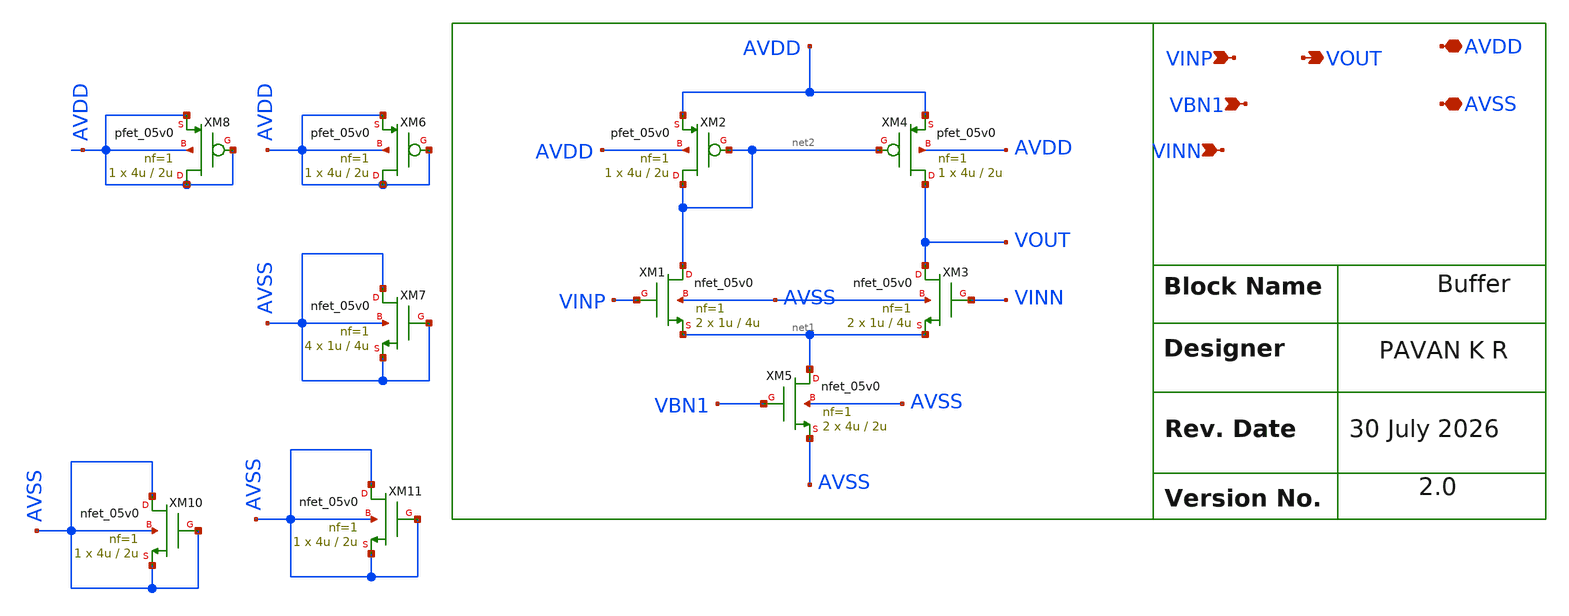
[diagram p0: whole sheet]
** sch_path: design/schematics/EIS/pkr_cic_bms_afe_eis_buffer.sch
**.subckt pkr_cic_bms_afe_eis_buffer VINP VOUT AVDD AVSS VBN1 VINN
*.ipin VINP
*.opin VOUT
*.iopin AVDD
*.iopin AVSS
*.ipin VBN1
*.ipin VINN
XM1 net2 VINP net1 AVSS nfet_05v0 L=4u W=1u nf=1 ad='int((nf+1)/2) * W/nf * 0.18u' as='int((nf+2)/2) * W/nf * 0.18u'
+ pd='2*int((nf+1)/2) * (W/nf + 0.18u)' ps='2*int((nf+2)/2) * (W/nf + 0.18u)' nrd='0.18u / W' nrs='0.18u / W'
+ sa=0 sb=0 sd=0 m=2
XM2 net2 net2 AVDD AVDD pfet_05v0 L=2u W=4u nf=1 ad='int((nf+1)/2) * W/nf * 0.18u' as='int((nf+2)/2) * W/nf * 0.18u'
+ pd='2*int((nf+1)/2) * (W/nf + 0.18u)' ps='2*int((nf+2)/2) * (W/nf + 0.18u)' nrd='0.18u / W' nrs='0.18u / W'
+ sa=0 sb=0 sd=0 m=1
XM3 VOUT VINN net1 AVSS nfet_05v0 L=4u W=1u nf=1 ad='int((nf+1)/2) * W/nf * 0.18u' as='int((nf+2)/2) * W/nf * 0.18u'
+ pd='2*int((nf+1)/2) * (W/nf + 0.18u)' ps='2*int((nf+2)/2) * (W/nf + 0.18u)' nrd='0.18u / W' nrs='0.18u / W'
+ sa=0 sb=0 sd=0 m=2
XM4 VOUT net2 AVDD AVDD pfet_05v0 L=2u W=4u nf=1 ad='int((nf+1)/2) * W/nf * 0.18u' as='int((nf+2)/2) * W/nf * 0.18u'
+ pd='2*int((nf+1)/2) * (W/nf + 0.18u)' ps='2*int((nf+2)/2) * (W/nf + 0.18u)' nrd='0.18u / W' nrs='0.18u / W'
+ sa=0 sb=0 sd=0 m=1
XM5 net1 VBN1 AVSS AVSS nfet_05v0 L=2u W=4u nf=1 ad='int((nf+1)/2) * W/nf * 0.18u' as='int((nf+2)/2) * W/nf * 0.18u'
+ pd='2*int((nf+1)/2) * (W/nf + 0.18u)' ps='2*int((nf+2)/2) * (W/nf + 0.18u)' nrd='0.18u / W' nrs='0.18u / W'
+ sa=0 sb=0 sd=0 m=2
XM7 AVSS AVSS AVSS AVSS nfet_05v0 L=4u W=1u nf=1 ad='int((nf+1)/2) * W/nf * 0.18u' as='int((nf+2)/2) * W/nf * 0.18u'
+ pd='2*int((nf+1)/2) * (W/nf + 0.18u)' ps='2*int((nf+2)/2) * (W/nf + 0.18u)' nrd='0.18u / W' nrs='0.18u / W'
+ sa=0 sb=0 sd=0 m=4
XM8 AVDD AVDD AVDD AVDD pfet_05v0 L=2u W=4u nf=1 ad='int((nf+1)/2) * W/nf * 0.18u' as='int((nf+2)/2) * W/nf * 0.18u'
+ pd='2*int((nf+1)/2) * (W/nf + 0.18u)' ps='2*int((nf+2)/2) * (W/nf + 0.18u)' nrd='0.18u / W' nrs='0.18u / W'
+ sa=0 sb=0 sd=0 m=1
XM6 AVDD AVDD AVDD AVDD pfet_05v0 L=2u W=4u nf=1 ad='int((nf+1)/2) * W/nf * 0.18u' as='int((nf+2)/2) * W/nf * 0.18u'
+ pd='2*int((nf+1)/2) * (W/nf + 0.18u)' ps='2*int((nf+2)/2) * (W/nf + 0.18u)' nrd='0.18u / W' nrs='0.18u / W'
+ sa=0 sb=0 sd=0 m=1
XM10 AVSS AVSS AVSS AVSS nfet_05v0 L=2u W=4u nf=1 ad='int((nf+1)/2) * W/nf * 0.18u' as='int((nf+2)/2) * W/nf * 0.18u'
+ pd='2*int((nf+1)/2) * (W/nf + 0.18u)' ps='2*int((nf+2)/2) * (W/nf + 0.18u)' nrd='0.18u / W' nrs='0.18u / W'
+ sa=0 sb=0 sd=0 m=1
XM11 AVSS AVSS AVSS AVSS nfet_05v0 L=2u W=4u nf=1 ad='int((nf+1)/2) * W/nf * 0.18u' as='int((nf+2)/2) * W/nf * 0.18u'
+ pd='2*int((nf+1)/2) * (W/nf + 0.18u)' ps='2*int((nf+2)/2) * (W/nf + 0.18u)' nrd='0.18u / W' nrs='0.18u / W'
+ sa=0 sb=0 sd=0 m=1
**.ends
.end
